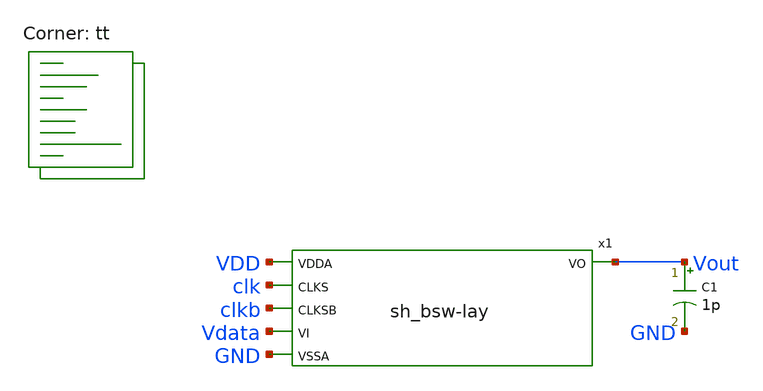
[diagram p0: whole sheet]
** sch_path: xschem/sh_bsw-lay-tb.sch
**.subckt sh_bsw-lay-tb
C1 Vout GND 1p m=1
x1 VDD clk clkb Vdata GND Vout sh_bsw-lay
**** begin user architecture code
 .lib $::SKYWATER_MODELS/sky130.lib.spice tt
.include $::SKYWATER_STDCELLS/sky130_fd_sc_hd.spice
.param mc_mm_switch = 0
.param mc_pr_switch = 0




  .include ~/sky130_projects/UNIC-CASS-2024/spice/sh_bsw-pex.spice
  .param fin=9.3e3 in_delay={10e-9}
  .param fclk={10*fin} tclk={1/fclk} thclk={tclk/2}
  .option wnflag=1
  .option safecurrents

  Vvdd  vdd   gnd 1.8
  Vdt   vdata gnd sin(0.5 0.5 {fin} {in_delay})
  Vclk  clk   gnd pulse(0 1.8 10e-9 1p 1p {thclk} {tclk})
  Vclkb clkb  gnd pulse(1.8 0 10e-9 1p 1p {thclk} {tclk})

  .control
     reset
     save all
     tran 10n 2m uic
     write sh_bsw-tb.raw
    quit 0
  .endc



**** end user architecture code
**.ends
.end
